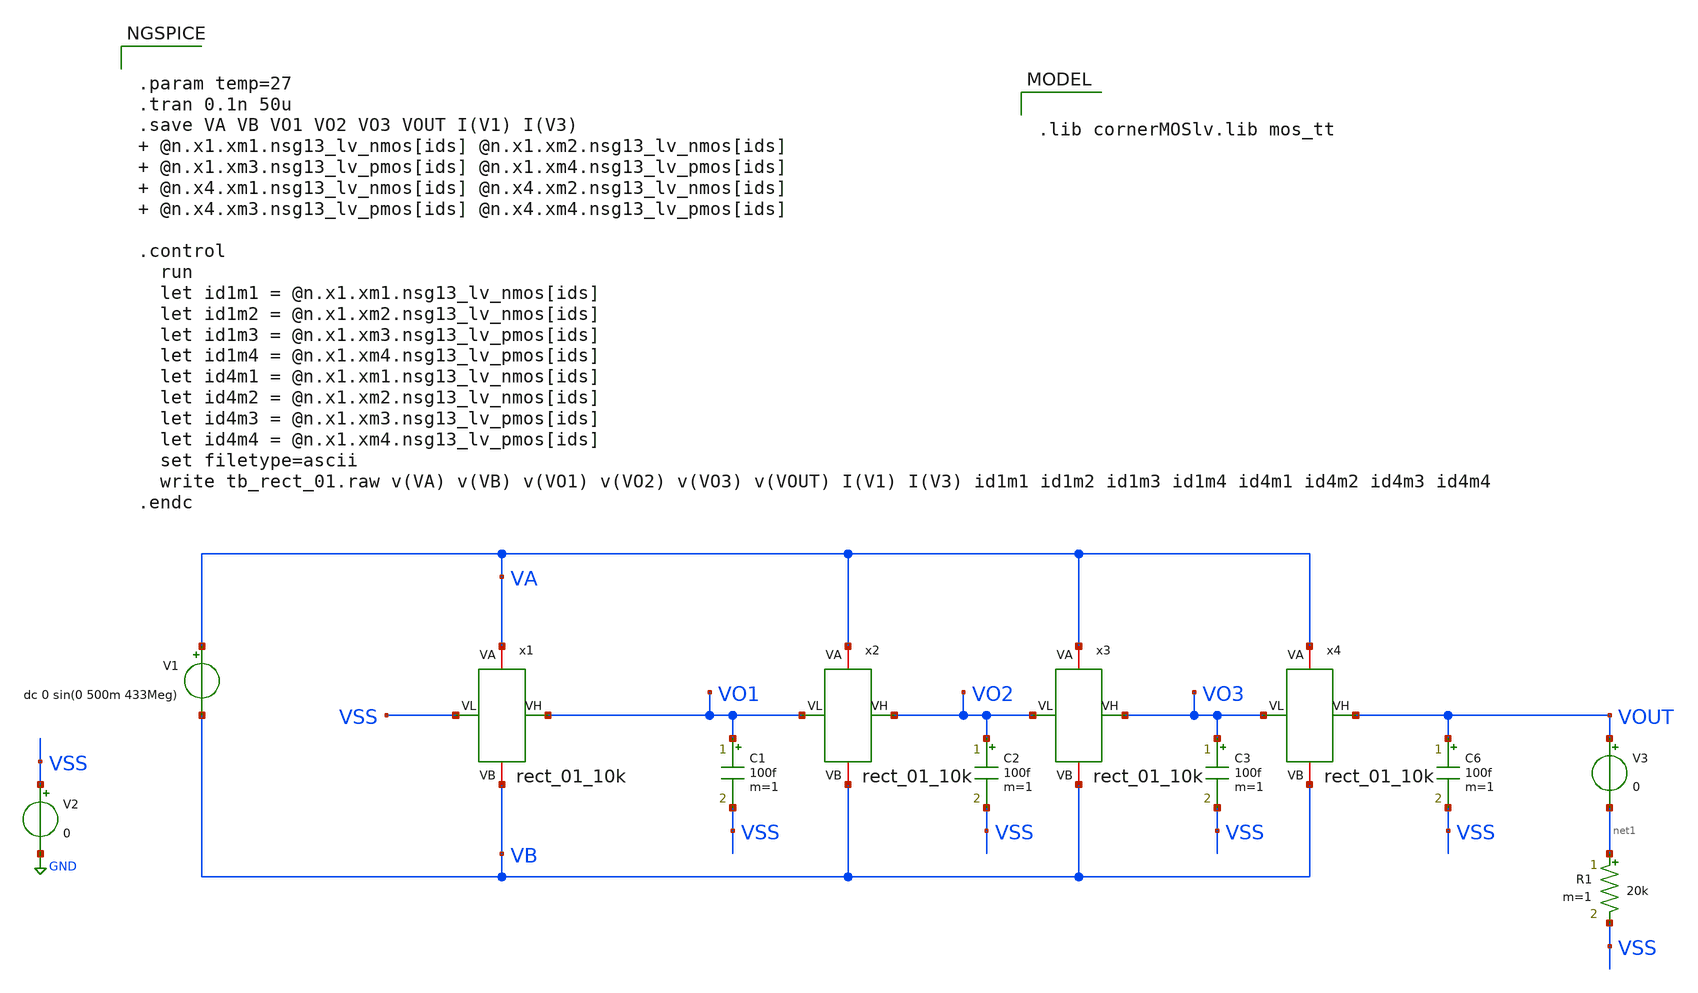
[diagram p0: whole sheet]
** sch_path: analog/tb/tb_rect_01.sch
**.subckt tb_rect_01
V1 VA VB dc 0 sin(0 500m 433Meg)
C1 VO1 VSS 100f m=1
V2 VSS GND 0
x1 VA VSS VO1 VB rect_01_10k
C2 VO2 VSS 100f m=1
x2 VA VO1 VO2 VB rect_01_10k
C3 VO3 VSS 100f m=1
x3 VA VO2 VO3 VB rect_01_10k
x4 VA VO3 VOUT VB rect_01_10k
C6 VOUT VSS 100f m=1
R1 net1 VSS 20k m=1
V3 VOUT net1 0
**** begin user architecture code


.param temp=27
.tran 0.1n 50u
.save VA VB VO1 VO2 VO3 VOUT I(V1) I(V3)  @n.x1.xm1.nsg13_lv_nmos[ids] @n.x1.xm2.nsg13_lv_nmos[ids]  @n.x1.xm3.nsg13_lv_pmos[ids] @n.x1.xm4.nsg13_lv_pmos[ids]  @n.x4.xm1.nsg13_lv_nmos[ids] @n.x4.xm2.nsg13_lv_nmos[ids]  @n.x4.xm3.nsg13_lv_pmos[ids] @n.x4.xm4.nsg13_lv_pmos[ids]

.control
  run
  let id1m1 = @n.x1.xm1.nsg13_lv_nmos[ids]
  let id1m2 = @n.x1.xm2.nsg13_lv_nmos[ids]
  let id1m3 = @n.x1.xm3.nsg13_lv_pmos[ids]
  let id1m4 = @n.x1.xm4.nsg13_lv_pmos[ids]
  let id4m1 = @n.x1.xm1.nsg13_lv_nmos[ids]
  let id4m2 = @n.x1.xm2.nsg13_lv_nmos[ids]
  let id4m3 = @n.x1.xm3.nsg13_lv_pmos[ids]
  let id4m4 = @n.x1.xm4.nsg13_lv_pmos[ids]
  set filetype=ascii
  write tb_rect_01.raw v(VA) v(VB) v(VO1) v(VO2) v(VO3) v(VOUT) I(V1) I(V3) id1m1 id1m2 id1m3 id1m4
+ id4m1 id4m2 id4m3 id4m4
.endc




.lib cornerMOSlv.lib mos_tt


**** end user architecture code
**.ends

* expanding   symbol:  rect_01_10k.sym # of pins=4
** sym_path: analog/core/rect_01_10k.sym
** sch_path: analog/core/rect_01_10k.sch
.subckt rect_01_10k VA VL VH VB
*.iopin VL
*.iopin VH
*.iopin VA
*.iopin VB
XM1 VL net1 net2 VL sg13_lv_nmos w=200u l=0.13u ng=40 m=1 mm_ok=1
XM3 VH net2 net1 VH sg13_lv_pmos w=400u l=0.13u ng=40 m=1 mm_ok=1
XM2 VL net2 net1 VL sg13_lv_nmos w=200u l=0.13u ng=40 m=1 mm_ok=1
XM4 VH net1 net2 VH sg13_lv_pmos w=400u l=0.13u ng=40 m=1 mm_ok=1
C1 VA net1 50p m=1
C2 net2 VB 50p m=1
.ends

.GLOBAL GND
.end
